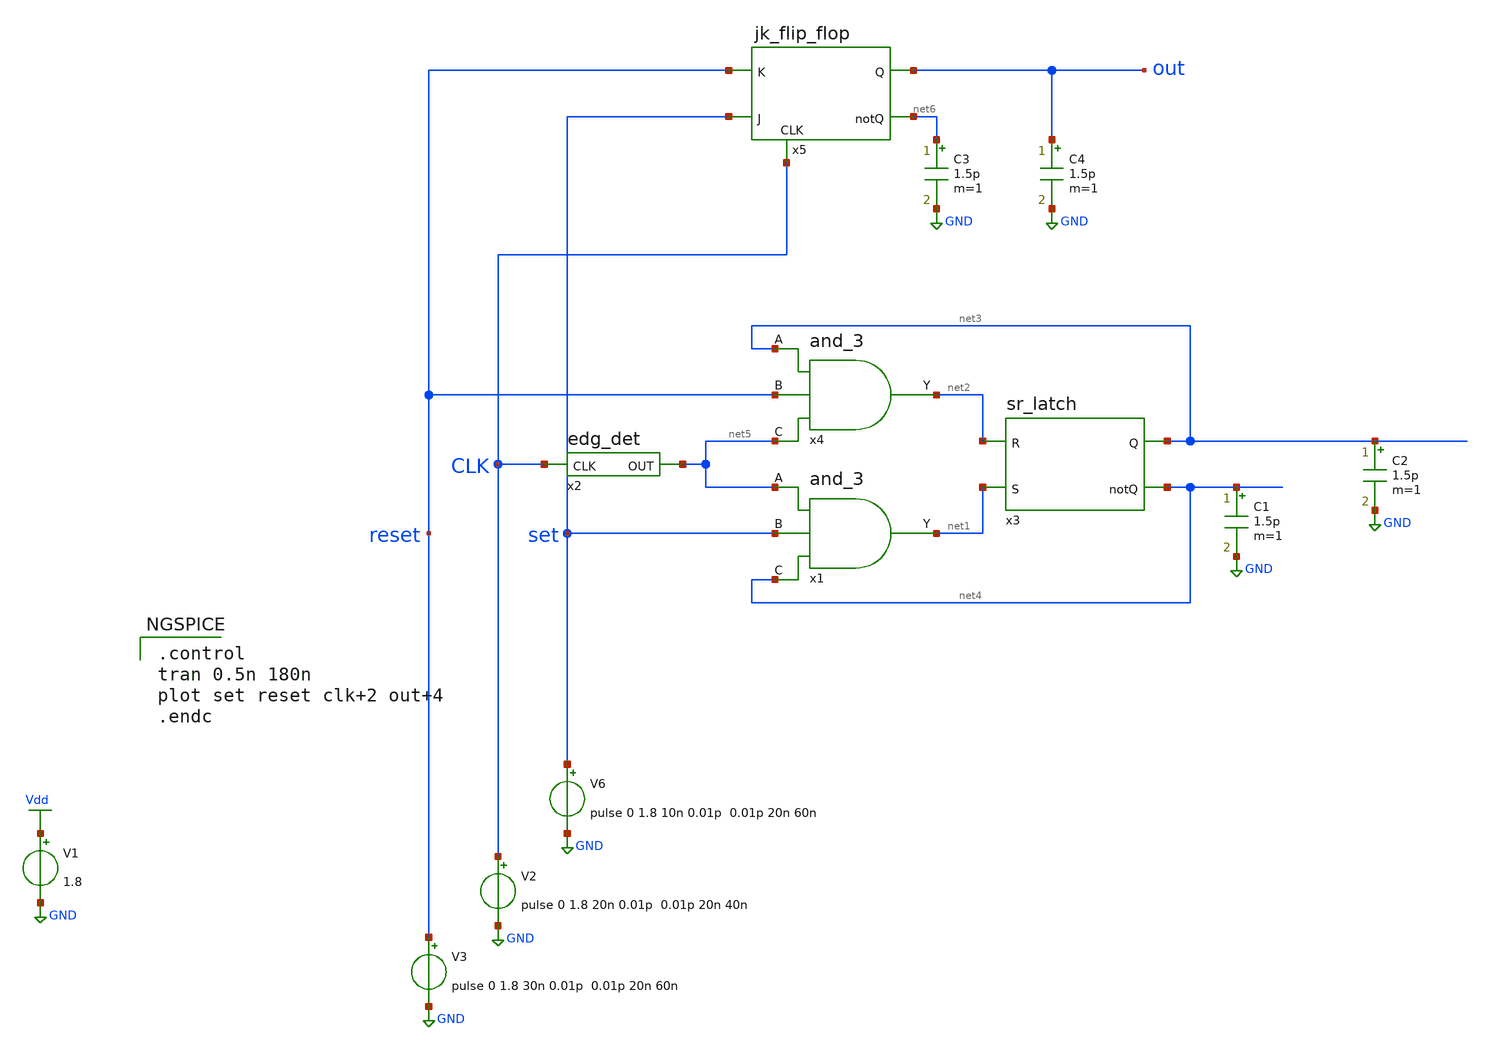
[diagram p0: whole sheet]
** sch_path: Circuiti/latch_demos_test2.sch
**.subckt latch_demos_test2
V1 Vdd GND 1.8
V6 set GND pulse 0 1.8 10n 0.01p 0.01p 20n 60n
x1 net5 net1 set net4 and_3
x4 net3 net2 reset net5 and_3
C1 net4 GND 1.5p m=1
C2 net3 GND 1.5p m=1
x3 net2 net3 net4 net1 sr_latch
V2 CLK GND pulse 0 1.8 20n 0.01p 0.01p 20n 40n
V3 reset GND pulse 0 1.8 30n 0.01p 0.01p 20n 60n
x2 net5 CLK edg_det
x5 reset out CLK net6 set jk_flip_flop
C3 net6 GND 1.5p m=1
C4 out GND 1.5p m=1
**** begin user architecture code


.lib /home/matteo/xschem_downloads/skywater-pdk/libraries/sky130_fd_pr_ngspice/latest/models/sky130.lib.spice tt

*.include /home/matteo/xschem_downloads/skywater-pdk/libraries/sky130_fd_pr_ngspice/latest/cells/nfet_01v8/sky130_fd_pr__nfet_01v8__tt.corner.spice

.param mc_mm_switch=0
.param mc_pr_switch=1



.control
tran 0.5n 180n
plot set reset clk+2 out+4
.endc


**** end user architecture code
**.ends

* expanding   symbol:  /home/matteo/Documenti/tesi/Circuiti/logic_gates_sch_sym/and_3.sym # of
*+ pins=4
** sym_path: Circuiti/logic_gates_sch_sym/and_3.sym
** sch_path: Circuiti/logic_gates_sch_sym/and_3.sch
.subckt and_3 A Y B C
*.ipin A
*.ipin B
*.ipin C
*.opin Y
x1 A Y net1 and_2
x2 B net1 C and_2
.ends


* expanding   symbol:  /home/matteo/Documenti/tesi/Circuiti/latches_sch_sym/sr_latch.sym # of pins=4
** sym_path: Circuiti/latches_sch_sym/sr_latch.sym
** sch_path: Circuiti/latches_sch_sym/sr_latch.sch
.subckt sr_latch R Q notQ S
*.ipin R
*.ipin S
*.opin Q
*.opin notQ
x1 R Q notQ nor_2
x2 Q notQ S nor_2
.ends


* expanding   symbol:  /home/matteo/Documenti/tesi/Circuiti/latches_sch_sym/edg_det.sym # of pins=2
** sym_path: Circuiti/latches_sch_sym/edg_det.sym
** sch_path: Circuiti/latches_sch_sym/edg_det.sch
.subckt edg_det OUT CLK
*.ipin CLK
*.opin OUT
x3 CLK net1 not
C3 net1 GND 1.5p m=1
x1 CLK OUT net1 and_2
.ends


* expanding   symbol:  /home/matteo/Documenti/tesi/Circuiti/latches_sch_sym/jk_flip_flop.sym # of
*+ pins=5
** sym_path: Circuiti/latches_sch_sym/jk_flip_flop.sym
** sch_path: Circuiti/latches_sch_sym/jk_flip_flop.sch
.subckt jk_flip_flop K Q CLK notQ J
*.ipin K
*.ipin J
*.opin Q
*.opin notQ
*.ipin CLK
x5 net2 Q notQ nor_2
x6 Q notQ net1 nor_2
x7 Q net2 K net3 and_3
x8 net3 net1 J notQ and_3
x9 CLK net4 not
x10 CLK net3 net4 and_2
C1 net4 GND 1.5p m=1
.ends


* expanding   symbol:  /home/matteo/Documenti/tesi/Circuiti/logic_gates_sch_sym/and_2.sym # of
*+ pins=3
** sym_path: Circuiti/logic_gates_sch_sym/and_2.sym
** sch_path: Circuiti/logic_gates_sch_sym/and_2.sch
.subckt and_2 A Y B
*.ipin B
*.ipin A
*.opin Y
x1 A net1 B nand_2
x2 net1 Y not
.ends


* expanding   symbol:  /home/matteo/Documenti/tesi/Circuiti/logic_gates_sch_sym/nor_2.sym # of
*+ pins=3
** sym_path: Circuiti/logic_gates_sch_sym/nor_2.sym
** sch_path: Circuiti/logic_gates_sch_sym/nor_2.sch
.subckt nor_2 A Y B
*.opin Y
*.ipin A
*.ipin B
XM1 Y B GND GND sky130_fd_pr__nfet_01v8 L=0.45 W=1 nf=1 ad='int((nf+1)/2) * W/nf * 0.29' as='int((nf+2)/2) * W/nf * 0.29'
+ pd='2*int((nf+1)/2) * (W/nf + 0.29)' ps='2*int((nf+2)/2) * (W/nf + 0.29)' nrd='0.29 / W' nrs='0.29 / W'
+ sa=0 sb=0 sd=0 mult=1 m=1
XM3 Y B net1 VDD sky130_fd_pr__pfet_01v8 L=0.15 W=4.8 nf=1 ad='int((nf+1)/2) * W/nf * 0.29' as='int((nf+2)/2) * W/nf * 0.29'
+ pd='2*int((nf+1)/2) * (W/nf + 0.29)' ps='2*int((nf+2)/2) * (W/nf + 0.29)' nrd='0.29 / W' nrs='0.29 / W'
+ sa=0 sb=0 sd=0 mult=1 m=1
XM4 net1 A Vdd VDD sky130_fd_pr__pfet_01v8 L=0.15 W=4.8 nf=1 ad='int((nf+1)/2) * W/nf * 0.29' as='int((nf+2)/2) * W/nf * 0.29'
+ pd='2*int((nf+1)/2) * (W/nf + 0.29)' ps='2*int((nf+2)/2) * (W/nf + 0.29)' nrd='0.29 / W' nrs='0.29 / W'
+ sa=0 sb=0 sd=0 mult=1 m=1
XM2 Y A GND GND sky130_fd_pr__nfet_01v8 L=0.45 W=1 nf=1 ad='int((nf+1)/2) * W/nf * 0.29' as='int((nf+2)/2) * W/nf * 0.29'
+ pd='2*int((nf+1)/2) * (W/nf + 0.29)' ps='2*int((nf+2)/2) * (W/nf + 0.29)' nrd='0.29 / W' nrs='0.29 / W'
+ sa=0 sb=0 sd=0 mult=1 m=1
.ends


* expanding   symbol:  /home/matteo/Documenti/tesi/Circuiti/logic_gates_sch_sym/not.sym # of pins=2
** sym_path: Circuiti/logic_gates_sch_sym/not.sym
** sch_path: Circuiti/logic_gates_sch_sym/not.sch
.subckt not A Y
*.ipin A
*.opin Y
XM1 Y A GND GND sky130_fd_pr__nfet_01v8 L=0.45 W=1 nf=1 ad='int((nf+1)/2) * W/nf * 0.29' as='int((nf+2)/2) * W/nf * 0.29'
+ pd='2*int((nf+1)/2) * (W/nf + 0.29)' ps='2*int((nf+2)/2) * (W/nf + 0.29)' nrd='0.29 / W' nrs='0.29 / W'
+ sa=0 sb=0 sd=0 mult=1 m=1
XM2 Y A Vdd VDD sky130_fd_pr__pfet_01v8 L=0.45 W=4.8 nf=1 ad='int((nf+1)/2) * W/nf * 0.29' as='int((nf+2)/2) * W/nf * 0.29'
+ pd='2*int((nf+1)/2) * (W/nf + 0.29)' ps='2*int((nf+2)/2) * (W/nf + 0.29)' nrd='0.29 / W' nrs='0.29 / W'
+ sa=0 sb=0 sd=0 mult=1 m=1
.ends


* expanding   symbol:  /home/matteo/Documenti/tesi/Circuiti/logic_gates_sch_sym/nand_2.sym # of
*+ pins=3
** sym_path: Circuiti/logic_gates_sch_sym/nand_2.sym
** sch_path: Circuiti/logic_gates_sch_sym/nand_2.sch
.subckt nand_2 A Y B
*.ipin A
*.ipin B
*.opin Y
XM1 Y A net1 GND sky130_fd_pr__nfet_01v8 L=0.15 W=1 nf=1 ad='int((nf+1)/2) * W/nf * 0.29' as='int((nf+2)/2) * W/nf * 0.29'
+ pd='2*int((nf+1)/2) * (W/nf + 0.29)' ps='2*int((nf+2)/2) * (W/nf + 0.29)' nrd='0.29 / W' nrs='0.29 / W'
+ sa=0 sb=0 sd=0 mult=1 m=1
XM3 Y B Vdd VDD sky130_fd_pr__pfet_01v8 L=0.45 W=4.8 nf=1 ad='int((nf+1)/2) * W/nf * 0.29' as='int((nf+2)/2) * W/nf * 0.29'
+ pd='2*int((nf+1)/2) * (W/nf + 0.29)' ps='2*int((nf+2)/2) * (W/nf + 0.29)' nrd='0.29 / W' nrs='0.29 / W'
+ sa=0 sb=0 sd=0 mult=1 m=1
XM4 Y A Vdd VDD sky130_fd_pr__pfet_01v8 L=0.45 W=4.8 nf=1 ad='int((nf+1)/2) * W/nf * 0.29' as='int((nf+2)/2) * W/nf * 0.29'
+ pd='2*int((nf+1)/2) * (W/nf + 0.29)' ps='2*int((nf+2)/2) * (W/nf + 0.29)' nrd='0.29 / W' nrs='0.29 / W'
+ sa=0 sb=0 sd=0 mult=1 m=1
XM2 net1 B GND GND sky130_fd_pr__nfet_01v8 L=0.15 W=1 nf=1 ad='int((nf+1)/2) * W/nf * 0.29' as='int((nf+2)/2) * W/nf * 0.29'
+ pd='2*int((nf+1)/2) * (W/nf + 0.29)' ps='2*int((nf+2)/2) * (W/nf + 0.29)' nrd='0.29 / W' nrs='0.29 / W'
+ sa=0 sb=0 sd=0 mult=1 m=1
.ends

.GLOBAL GND
.GLOBAL Vdd
.end
